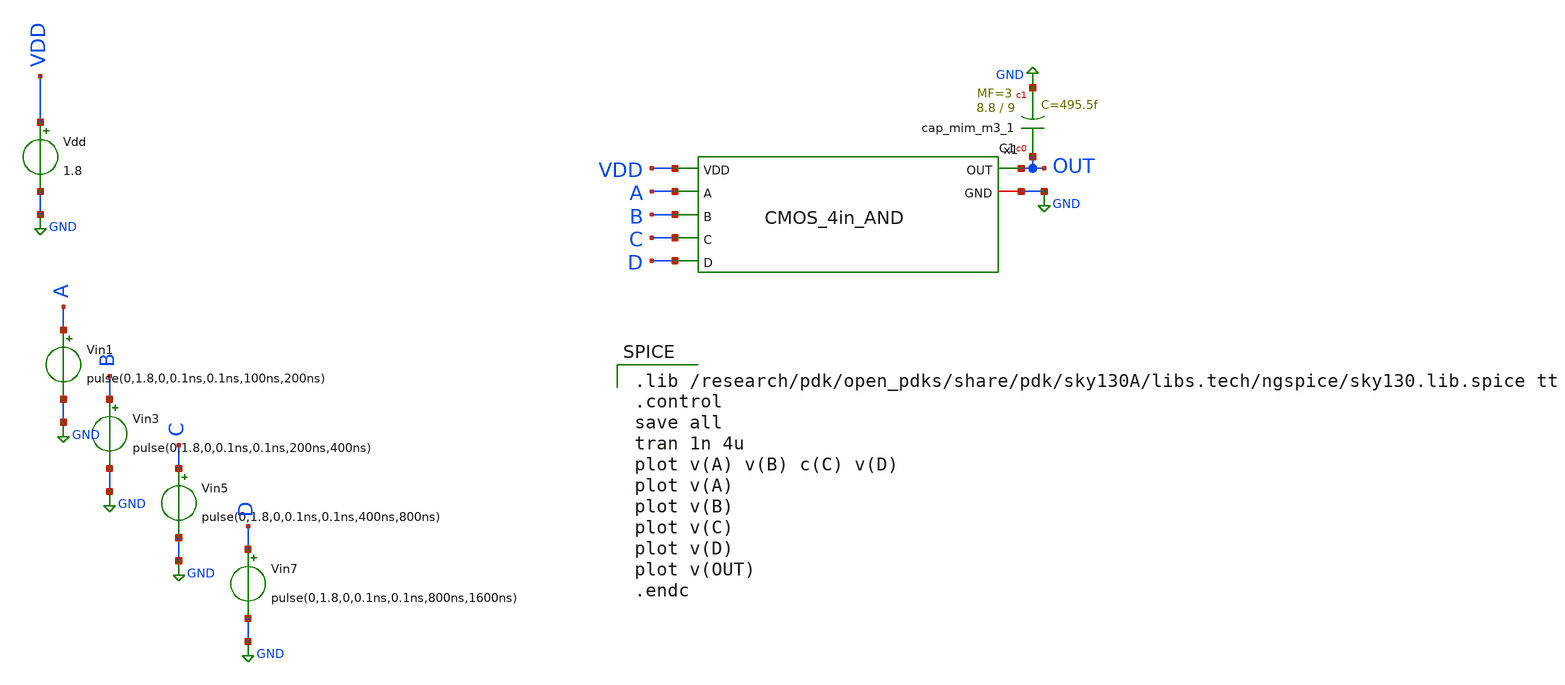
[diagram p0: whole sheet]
** sch_path: skywater_stuff/CMOS_4in_AND_sim.sch
**.subckt CMOS_4in_AND_sim
Vin1 A GND pulse(0,1.8,0,0.1ns,0.1ns,100ns,200ns)
Vin3 B GND pulse(0,1.8,0,0.1ns,0.1ns,200ns,400ns)
Vin5 C GND pulse(0,1.8,0,0.1ns,0.1ns,400ns,800ns)
Vin7 D GND pulse(0,1.8,0,0.1ns,0.1ns,800ns,1600ns)
Vdd VDD GND 1.8
x1 A B C D OUT GND VDD CMOS_4in_AND
XC1 OUT GND sky130_fd_pr__cap_mim_m3_1 W=8.8 L=9 MF=3 m=3
**** begin user architecture code

.lib /research/pdk/open_pdks/share/pdk/sky130A/libs.tech/ngspice/sky130.lib.spice tt
.control
save all
tran 1n 4u
plot v(A) v(B) c(C) v(D)
plot v(A)
plot v(B)
plot v(C)
plot v(D)
plot v(OUT)
.endc


**** end user architecture code
**.ends

* expanding   symbol:  CMOS_4in_AND.sym # of pins=7
** sym_path: skywater_stuff/CMOS_4in_AND.sym
** sch_path: skywater_stuff/CMOS_4in_AND.sch
.subckt CMOS_4in_AND A B C D OUT GND VDD
*.ipin A
*.ipin B
*.ipin C
*.ipin D
*.opin OUT
*.iopin GND
*.ipin VDD
XM3 net1 B VDD VDD sky130_fd_pr__pfet_01v8 L=0.15 W=3 nf=1 ad='int((nf+1)/2) * W/nf * 0.29' as='int((nf+2)/2) * W/nf * 0.29'
+ pd='2*int((nf+1)/2) * (W/nf + 0.29)' ps='2*int((nf+2)/2) * (W/nf + 0.29)' nrd='0.29 / W' nrs='0.29 / W'
+ sa=0 sb=0 sd=0 mult=1 m=1
XM4 net1 C VDD VDD sky130_fd_pr__pfet_01v8 L=0.15 W=3 nf=1 ad='int((nf+1)/2) * W/nf * 0.29' as='int((nf+2)/2) * W/nf * 0.29'
+ pd='2*int((nf+1)/2) * (W/nf + 0.29)' ps='2*int((nf+2)/2) * (W/nf + 0.29)' nrd='0.29 / W' nrs='0.29 / W'
+ sa=0 sb=0 sd=0 mult=1 m=1
XM6 net2 B net3 GND sky130_fd_pr__nfet_01v8 L=0.15 W=1.5 nf=1 ad='int((nf+1)/2) * W/nf * 0.29' as='int((nf+2)/2) * W/nf * 0.29'
+ pd='2*int((nf+1)/2) * (W/nf + 0.29)' ps='2*int((nf+2)/2) * (W/nf + 0.29)' nrd='0.29 / W' nrs='0.29 / W'
+ sa=0 sb=0 sd=0 mult=1 m=1
XM7 net3 C net4 GND sky130_fd_pr__nfet_01v8 L=0.15 W=1.5 nf=1 ad='int((nf+1)/2) * W/nf * 0.29' as='int((nf+2)/2) * W/nf * 0.29'
+ pd='2*int((nf+1)/2) * (W/nf + 0.29)' ps='2*int((nf+2)/2) * (W/nf + 0.29)' nrd='0.29 / W' nrs='0.29 / W'
+ sa=0 sb=0 sd=0 mult=1 m=1
XM8 net4 D GND GND sky130_fd_pr__nfet_01v8 L=0.15 W=1.5 nf=1 ad='int((nf+1)/2) * W/nf * 0.29' as='int((nf+2)/2) * W/nf * 0.29'
+ pd='2*int((nf+1)/2) * (W/nf + 0.29)' ps='2*int((nf+2)/2) * (W/nf + 0.29)' nrd='0.29 / W' nrs='0.29 / W'
+ sa=0 sb=0 sd=0 mult=1 m=1
XM9 OUT net1 GND GND sky130_fd_pr__nfet_01v8 L=0.15 W=1.5 nf=1 ad='int((nf+1)/2) * W/nf * 0.29' as='int((nf+2)/2) * W/nf * 0.29'
+ pd='2*int((nf+1)/2) * (W/nf + 0.29)' ps='2*int((nf+2)/2) * (W/nf + 0.29)' nrd='0.29 / W' nrs='0.29 / W'
+ sa=0 sb=0 sd=0 mult=1 m=1
XM10 OUT net1 VDD VDD sky130_fd_pr__pfet_01v8 L=0.15 W=3 nf=1 ad='int((nf+1)/2) * W/nf * 0.29' as='int((nf+2)/2) * W/nf * 0.29'
+ pd='2*int((nf+1)/2) * (W/nf + 0.29)' ps='2*int((nf+2)/2) * (W/nf + 0.29)' nrd='0.29 / W' nrs='0.29 / W'
+ sa=0 sb=0 sd=0 mult=1 m=1
XM1 net1 A net2 GND sky130_fd_pr__nfet_01v8 L=0.15 W=1.5 nf=1 ad='int((nf+1)/2) * W/nf * 0.29' as='int((nf+2)/2) * W/nf * 0.29'
+ pd='2*int((nf+1)/2) * (W/nf + 0.29)' ps='2*int((nf+2)/2) * (W/nf + 0.29)' nrd='0.29 / W' nrs='0.29 / W'
+ sa=0 sb=0 sd=0 mult=1 m=1
XM2 net1 A VDD VDD sky130_fd_pr__pfet_01v8 L=0.15 W=3 nf=1 ad='int((nf+1)/2) * W/nf * 0.29' as='int((nf+2)/2) * W/nf * 0.29'
+ pd='2*int((nf+1)/2) * (W/nf + 0.29)' ps='2*int((nf+2)/2) * (W/nf + 0.29)' nrd='0.29 / W' nrs='0.29 / W'
+ sa=0 sb=0 sd=0 mult=1 m=1
XM5 net1 D VDD VDD sky130_fd_pr__pfet_01v8 L=0.15 W=3 nf=1 ad='int((nf+1)/2) * W/nf * 0.29' as='int((nf+2)/2) * W/nf * 0.29'
+ pd='2*int((nf+1)/2) * (W/nf + 0.29)' ps='2*int((nf+2)/2) * (W/nf + 0.29)' nrd='0.29 / W' nrs='0.29 / W'
+ sa=0 sb=0 sd=0 mult=1 m=1
.ends

.GLOBAL GND
.end
